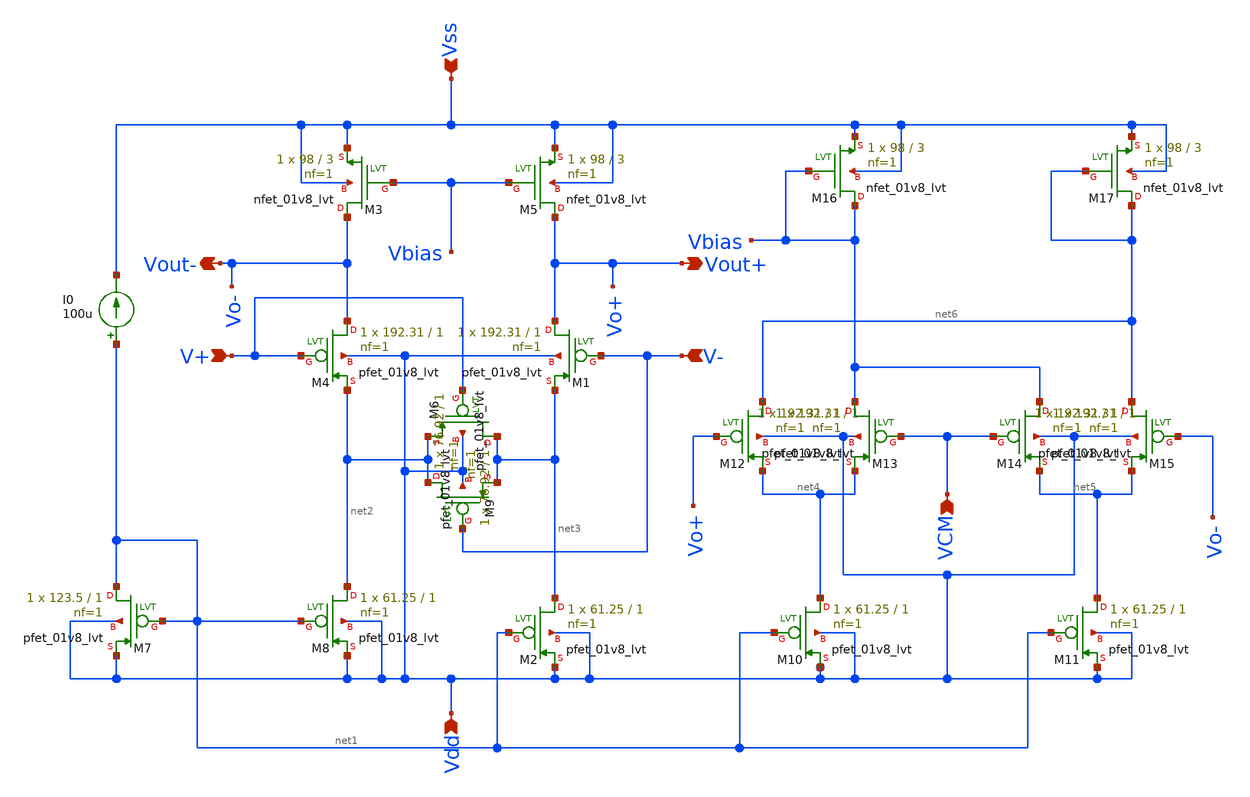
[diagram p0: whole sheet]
** sch_path: xschem/untitled-7.sch
**.subckt untitled-7 Vout+ Vdd Vss V+ V- Vout- VCM
*.opin Vout+
*.ipin Vdd
*.ipin Vss
*.ipin V+
*.ipin V-
*.opin Vout-
*.ipin VCM
I0 net1 Vss 100u
XM7 net1 net1 Vdd Vdd sky130_fd_pr__pfet_01v8_lvt L=1 W=123.5 nf=1 ad='int((1 + 1)/2) * 123.5 / 1 * 0.29'
+ as='int((1 + 2)/2) * 123.5 / 1 * 0.29' pd='2*int((1 + 1)/2) * (123.5 / 1 + 0.29)' ps='2*int((1 + 2)/2) * (123.5 / 1 + 0.29)'
+ nrd='0.29 / 123.5 ' nrs='0.29 / 123.5 ' sa=0 sb=0 sd=0 mult=1 m=1
XM8 net2 net1 Vdd Vdd sky130_fd_pr__pfet_01v8_lvt L=1 W=61.25 nf=1 ad='int((1 + 1)/2) * 61.25 / 1 * 0.29'
+ as='int((1 + 2)/2) * 61.25 / 1 * 0.29' pd='2*int((1 + 1)/2) * (61.25 / 1 + 0.29)' ps='2*int((1 + 2)/2) * (61.25 / 1 + 0.29)'
+ nrd='0.29 / 61.25 ' nrs='0.29 / 61.25 ' sa=0 sb=0 sd=0 mult=1 m=1
XM4 Vout- V+ net2 Vdd sky130_fd_pr__pfet_01v8_lvt L=1 W=192.31 nf=1 ad='int((1 + 1)/2) * 192.31 / 1 * 0.29'
+ as='int((1 + 2)/2) * 192.31 / 1 * 0.29' pd='2*int((1 + 1)/2) * (192.31 / 1 + 0.29)' ps='2*int((1 + 2)/2) * (192.31 / 1 + 0.29)'
+ nrd='0.29 / 192.31 ' nrs='0.29 / 192.31 ' sa=0 sb=0 sd=0 mult=1 m=1
XM1 Vout+ V- net3 Vdd sky130_fd_pr__pfet_01v8_lvt L=1 W=192.31 nf=1 ad='int((1 + 1)/2) * 192.31 / 1 * 0.29'
+ as='int((1 + 2)/2) * 192.31 / 1 * 0.29' pd='2*int((1 + 1)/2) * (192.31 / 1 + 0.29)' ps='2*int((1 + 2)/2) * (192.31 / 1 + 0.29)'
+ nrd='0.29 / 192.31 ' nrs='0.29 / 192.31 ' sa=0 sb=0 sd=0 mult=1 m=1
XM5 Vout+ Vbias Vss Vss sky130_fd_pr__nfet_01v8_lvt L=3 W=98 nf=1 ad='int((1 + 1)/2) * 98 / 1 * 0.29'
+ as='int((1 + 2)/2) * 98 / 1 * 0.29' pd='2*int((1 + 1)/2) * (98 / 1 + 0.29)' ps='2*int((1 + 2)/2) * (98 / 1 + 0.29)'
+ nrd='0.29 / 98 ' nrs='0.29 / 98 ' sa=0 sb=0 sd=0 mult=1 m=1
XM3 Vout- Vbias Vss Vss sky130_fd_pr__nfet_01v8_lvt L=3 W=98 nf=1 ad='int((1 + 1)/2) * 98 / 1 * 0.29'
+ as='int((1 + 2)/2) * 98 / 1 * 0.29' pd='2*int((1 + 1)/2) * (98 / 1 + 0.29)' ps='2*int((1 + 2)/2) * (98 / 1 + 0.29)'
+ nrd='0.29 / 98 ' nrs='0.29 / 98 ' sa=0 sb=0 sd=0 mult=1 m=1
XM2 net3 net1 Vdd Vdd sky130_fd_pr__pfet_01v8_lvt L=1 W=61.25 nf=1 ad='int((1 + 1)/2) * 61.25 / 1 * 0.29'
+ as='int((1 + 2)/2) * 61.25 / 1 * 0.29' pd='2*int((1 + 1)/2) * (61.25 / 1 + 0.29)' ps='2*int((1 + 2)/2) * (61.25 / 1 + 0.29)'
+ nrd='0.29 / 61.25 ' nrs='0.29 / 61.25 ' sa=0 sb=0 sd=0 mult=1 m=1
XM6 net3 V+ net2 Vdd sky130_fd_pr__pfet_01v8_lvt L=1 W=76.92 nf=1 ad='int((1 + 1)/2) * 76.92 / 1 * 0.29'
+ as='int((1 + 2)/2) * 76.92 / 1 * 0.29' pd='2*int((1 + 1)/2) * (76.92 / 1 + 0.29)' ps='2*int((1 + 2)/2) * (76.92 / 1 + 0.29)'
+ nrd='0.29 / 76.92 ' nrs='0.29 / 76.92 ' sa=0 sb=0 sd=0 mult=1 m=1
XM9 net2 V- net3 Vdd sky130_fd_pr__pfet_01v8_lvt L=1 W=76.92 nf=1 ad='int((1 + 1)/2) * 76.92 / 1 * 0.29'
+ as='int((1 + 2)/2) * 76.92 / 1 * 0.29' pd='2*int((1 + 1)/2) * (76.92 / 1 + 0.29)' ps='2*int((1 + 2)/2) * (76.92 / 1 + 0.29)'
+ nrd='0.29 / 76.92 ' nrs='0.29 / 76.92 ' sa=0 sb=0 sd=0 mult=1 m=1
XM10 net4 net1 Vdd Vdd sky130_fd_pr__pfet_01v8_lvt L=1 W=61.25 nf=1 ad='int((1 + 1)/2) * 61.25 / 1 * 0.29'
+ as='int((1 + 2)/2) * 61.25 / 1 * 0.29' pd='2*int((1 + 1)/2) * (61.25 / 1 + 0.29)' ps='2*int((1 + 2)/2) * (61.25 / 1 + 0.29)'
+ nrd='0.29 / 61.25 ' nrs='0.29 / 61.25 ' sa=0 sb=0 sd=0 mult=1 m=1
XM11 net5 net1 Vdd Vdd sky130_fd_pr__pfet_01v8_lvt L=1 W=61.25 nf=1 ad='int((1 + 1)/2) * 61.25 / 1 * 0.29'
+ as='int((1 + 2)/2) * 61.25 / 1 * 0.29' pd='2*int((1 + 1)/2) * (61.25 / 1 + 0.29)' ps='2*int((1 + 2)/2) * (61.25 / 1 + 0.29)'
+ nrd='0.29 / 61.25 ' nrs='0.29 / 61.25 ' sa=0 sb=0 sd=0 mult=1 m=1
XM12 net6 Vo+ net4 Vdd sky130_fd_pr__pfet_01v8_lvt L=1 W=192.31 nf=1 ad='int((1 + 1)/2) * 192.31 / 1 * 0.29'
+ as='int((1 + 2)/2) * 192.31 / 1 * 0.29' pd='2*int((1 + 1)/2) * (192.31 / 1 + 0.29)' ps='2*int((1 + 2)/2) * (192.31 / 1 + 0.29)'
+ nrd='0.29 / 192.31 ' nrs='0.29 / 192.31 ' sa=0 sb=0 sd=0 mult=1 m=1
XM13 Vbias VCM net4 Vdd sky130_fd_pr__pfet_01v8_lvt L=1 W=192.31 nf=1 ad='int((1 + 1)/2) * 192.31 / 1 * 0.29'
+ as='int((1 + 2)/2) * 192.31 / 1 * 0.29' pd='2*int((1 + 1)/2) * (192.31 / 1 + 0.29)' ps='2*int((1 + 2)/2) * (192.31 / 1 + 0.29)'
+ nrd='0.29 / 192.31 ' nrs='0.29 / 192.31 ' sa=0 sb=0 sd=0 mult=1 m=1
XM14 Vbias VCM net5 Vdd sky130_fd_pr__pfet_01v8_lvt L=1 W=192.31 nf=1 ad='int((1 + 1)/2) * 192.31 / 1 * 0.29'
+ as='int((1 + 2)/2) * 192.31 / 1 * 0.29' pd='2*int((1 + 1)/2) * (192.31 / 1 + 0.29)' ps='2*int((1 + 2)/2) * (192.31 / 1 + 0.29)'
+ nrd='0.29 / 192.31 ' nrs='0.29 / 192.31 ' sa=0 sb=0 sd=0 mult=1 m=1
XM15 net6 Vo- net5 Vdd sky130_fd_pr__pfet_01v8_lvt L=1 W=192.31 nf=1 ad='int((1 + 1)/2) * 192.31 / 1 * 0.29'
+ as='int((1 + 2)/2) * 192.31 / 1 * 0.29' pd='2*int((1 + 1)/2) * (192.31 / 1 + 0.29)' ps='2*int((1 + 2)/2) * (192.31 / 1 + 0.29)'
+ nrd='0.29 / 192.31 ' nrs='0.29 / 192.31 ' sa=0 sb=0 sd=0 mult=1 m=1
XM16 Vbias Vbias Vss Vss sky130_fd_pr__nfet_01v8_lvt L=3 W=98 nf=1 ad='int((1 + 1)/2) * 98 / 1 * 0.29'
+ as='int((1 + 2)/2) * 98 / 1 * 0.29' pd='2*int((1 + 1)/2) * (98 / 1 + 0.29)' ps='2*int((1 + 2)/2) * (98 / 1 + 0.29)'
+ nrd='0.29 / 98 ' nrs='0.29 / 98 ' sa=0 sb=0 sd=0 mult=1 m=1
XM17 net6 net6 Vss Vss sky130_fd_pr__nfet_01v8_lvt L=3 W=98 nf=1 ad='int((1 + 1)/2) * 98 / 1 * 0.29'
+ as='int((1 + 2)/2) * 98 / 1 * 0.29' pd='2*int((1 + 1)/2) * (98 / 1 + 0.29)' ps='2*int((1 + 2)/2) * (98 / 1 + 0.29)'
+ nrd='0.29 / 98 ' nrs='0.29 / 98 ' sa=0 sb=0 sd=0 mult=1 m=1
**.ends
.end
